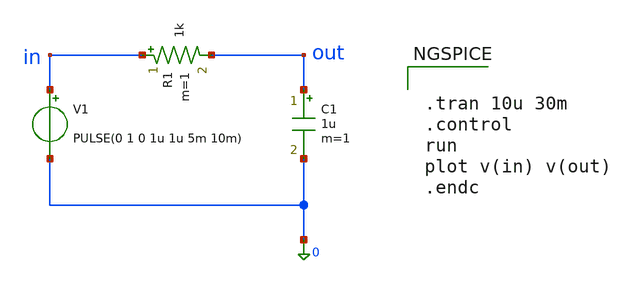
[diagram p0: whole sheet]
** sch_path: test_xschem/test.sch
**.subckt test
V1 in 0 PULSE(0 1 0 1u 1u 5m 10m)
R1 in out 1k m=1
C1 out 0 1u m=1
**** begin user architecture code


.tran 10u 30m
.control
run
plot v(in) v(out)
.endc


**** end user architecture code
**.ends
.end
